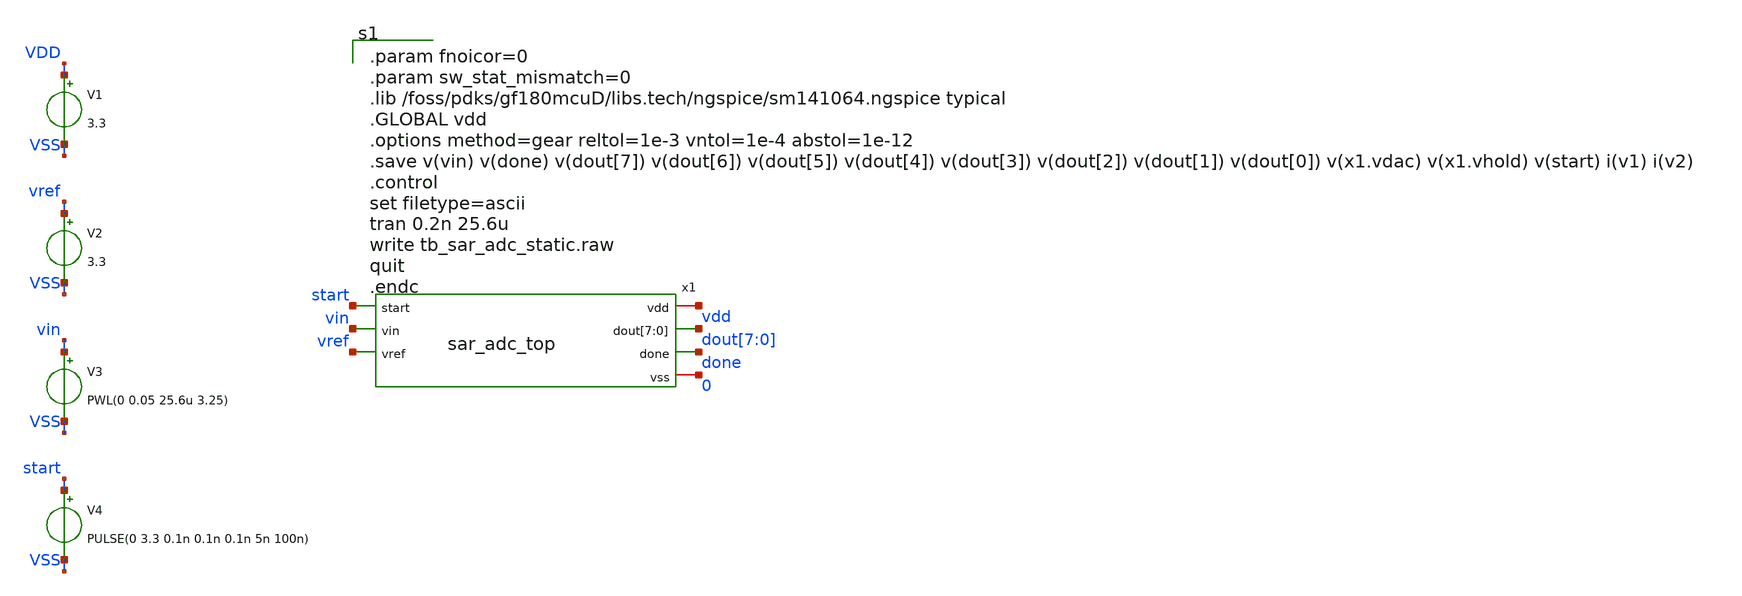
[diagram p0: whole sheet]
** sch_path: xschem/sar_adc/tb_sar_adc_static.sch
**.subckt tb_sar_adc_static
V1 VDD VSS 3.3
V2 vref VSS 3.3
V3 vin VSS PWL(0 0.05 25.6u 3.25)
V4 start VSS PULSE(0 3.3 0.1n 0.1n 0.1n 5n 100n)
x1 vdd start vin dout[7] dout[6] dout[5] dout[4] dout[3] dout[2] dout[1] dout[0] done vref 0
+ sar_adc_top
**.ends
**** begin user architecture code

.param fnoicor=0
.param sw_stat_mismatch=0
.lib /foss/pdks/gf180mcuD/libs.tech/ngspice/sm141064.ngspice typical
.GLOBAL vdd
.options method=gear reltol=1e-3 vntol=1e-4 abstol=1e-12
.save v(vin) v(done) v(dout[7]) v(dout[6]) v(dout[5]) v(dout[4]) v(dout[3]) v(dout[2]) v(dout[1]) v(dout[0]) v(x1.vdac) v(x1.vhold) v(start) i(v1) i(v2)
.control
set filetype=ascii
tran 0.2n 25.6u
write tb_sar_adc_static.raw
quit
.endc

**** end user architecture code
.end
